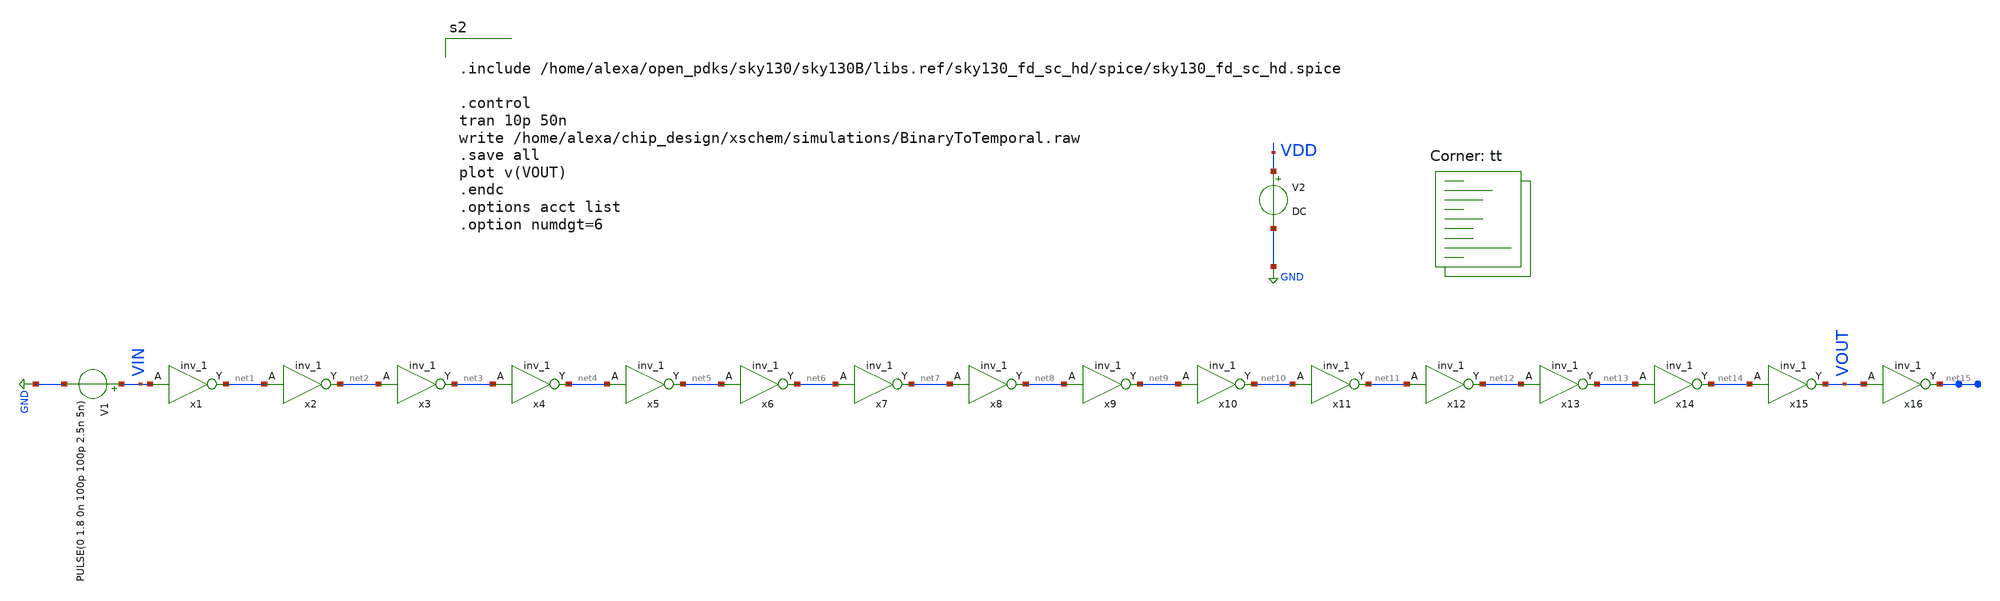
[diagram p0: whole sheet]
** sch_path: xschem/projects/InverterTest.sch
**.subckt InverterTest
V1 VIN GND PULSE(0 1.8 0n 100p 100p 2.5n 5n)
V2 VDD GND DC
x1 VIN 0 0 VDD VDD net1 sky130_fd_sc_hd__inv_1
x2 net1 0 0 VDD VDD net2 sky130_fd_sc_hd__inv_1
x3 net2 0 0 VDD VDD net3 sky130_fd_sc_hd__inv_1
x4 net3 0 0 VDD VDD net4 sky130_fd_sc_hd__inv_1
x5 net4 0 0 VDD VDD net5 sky130_fd_sc_hd__inv_1
x6 net5 0 0 VDD VDD net6 sky130_fd_sc_hd__inv_1
x7 net6 0 0 VDD VDD net7 sky130_fd_sc_hd__inv_1
x8 net7 0 0 VDD VDD net8 sky130_fd_sc_hd__inv_1
x9 net8 0 0 VDD VDD net9 sky130_fd_sc_hd__inv_1
x10 net9 0 0 VDD VDD net10 sky130_fd_sc_hd__inv_1
x11 net10 0 0 VDD VDD net11 sky130_fd_sc_hd__inv_1
x12 net11 0 0 VDD VDD net12 sky130_fd_sc_hd__inv_1
x13 net12 0 0 VDD VDD net13 sky130_fd_sc_hd__inv_1
x14 net13 0 0 VDD VDD net14 sky130_fd_sc_hd__inv_1
x15 net14 0 0 VDD VDD VOUT sky130_fd_sc_hd__inv_1
x16 VOUT 0 0 VDD VDD net15 sky130_fd_sc_hd__inv_1
**** begin user architecture code


.include /home/alexa/open_pdks/sky130/sky130B/libs.ref/sky130_fd_sc_hd/spice/sky130_fd_sc_hd.spice

.control
tran 10p 50n
write /home/alexa/chip_design/xschem/simulations/BinaryToTemporal.raw
.save all
plot v(VOUT)
.endc
.options acct list
.option numdgt=6


.lib $::SKYWATER_MODELS/sky130.lib.spice tt
**** end user architecture code
**.ends
.GLOBAL GND
.end
